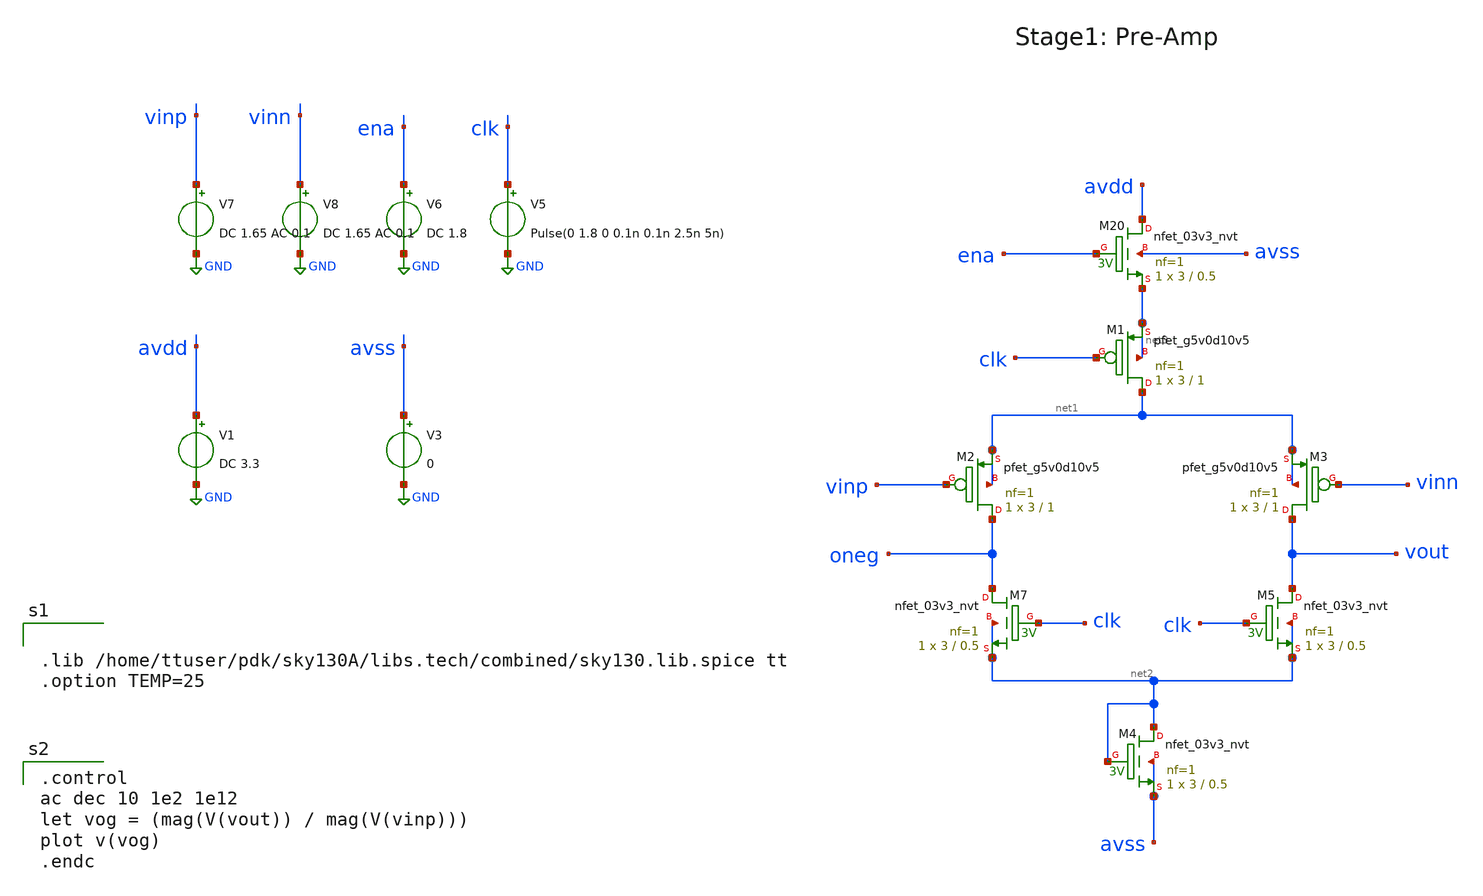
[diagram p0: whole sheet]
** sch_path: xschem/preamp.sch
**.subckt preamp
XM1 net1 clk net3 net3 sky130_fd_pr__pfet_g5v0d10v5 L=1 W=3 nf=1 ad='int((nf+1)/2) * W/nf * 0.29' as='int((nf+2)/2) * W/nf * 0.29'
+ pd='2*int((nf+1)/2) * (W/nf + 0.29)' ps='2*int((nf+2)/2) * (W/nf + 0.29)' nrd='0.29 / W' nrs='0.29 / W'
+ sa=0 sb=0 sd=0 mult=1 m=1
XM2 oneg vinp net1 net1 sky130_fd_pr__pfet_g5v0d10v5 L=1 W=3 nf=1 ad='int((nf+1)/2) * W/nf * 0.29' as='int((nf+2)/2) * W/nf * 0.29'
+ pd='2*int((nf+1)/2) * (W/nf + 0.29)' ps='2*int((nf+2)/2) * (W/nf + 0.29)' nrd='0.29 / W' nrs='0.29 / W'
+ sa=0 sb=0 sd=0 mult=1 m=1
XM3 vout vinn net1 net1 sky130_fd_pr__pfet_g5v0d10v5 L=1 W=3 nf=1 ad='int((nf+1)/2) * W/nf * 0.29' as='int((nf+2)/2) * W/nf * 0.29'
+ pd='2*int((nf+1)/2) * (W/nf + 0.29)' ps='2*int((nf+2)/2) * (W/nf + 0.29)' nrd='0.29 / W' nrs='0.29 / W'
+ sa=0 sb=0 sd=0 mult=1 m=1
XM7 oneg clk net2 net2 sky130_fd_pr__nfet_03v3_nvt L=0.5 W=3 nf=1 ad='int((nf+1)/2) * W/nf * 0.29' as='int((nf+2)/2) * W/nf * 0.29'
+ pd='2*int((nf+1)/2) * (W/nf + 0.29)' ps='2*int((nf+2)/2) * (W/nf + 0.29)' nrd='0.29 / W' nrs='0.29 / W'
+ sa=0 sb=0 sd=0 mult=1 m=1
XM5 vout clk net2 net2 sky130_fd_pr__nfet_03v3_nvt L=0.5 W=3 nf=1 ad='int((nf+1)/2) * W/nf * 0.29' as='int((nf+2)/2) * W/nf * 0.29'
+ pd='2*int((nf+1)/2) * (W/nf + 0.29)' ps='2*int((nf+2)/2) * (W/nf + 0.29)' nrd='0.29 / W' nrs='0.29 / W'
+ sa=0 sb=0 sd=0 mult=1 m=1
XM4 net2 net2 avss avss sky130_fd_pr__nfet_03v3_nvt L=0.5 W=3 nf=1 ad='int((nf+1)/2) * W/nf * 0.29' as='int((nf+2)/2) * W/nf * 0.29'
+ pd='2*int((nf+1)/2) * (W/nf + 0.29)' ps='2*int((nf+2)/2) * (W/nf + 0.29)' nrd='0.29 / W' nrs='0.29 / W'
+ sa=0 sb=0 sd=0 mult=1 m=1
XM20 avdd ena net3 avss sky130_fd_pr__nfet_03v3_nvt L=0.5 W=3 nf=1 ad='int((nf+1)/2) * W/nf * 0.29' as='int((nf+2)/2) * W/nf * 0.29'
+ pd='2*int((nf+1)/2) * (W/nf + 0.29)' ps='2*int((nf+2)/2) * (W/nf + 0.29)' nrd='0.29 / W' nrs='0.29 / W'
+ sa=0 sb=0 sd=0 mult=1 m=1
V1 avdd GND DC 3.3
V3 avss GND 0
V5 clk GND Pulse(0 1.8 0 0.1n 0.1n 2.5n 5n)
V6 ena GND DC 1.8
V7 vinp GND DC 1.65 AC 0.1
V8 vinn GND DC 1.65 AC 0.1
**** begin user architecture code


.lib /home/ttuser/pdk/sky130A/libs.tech/combined/sky130.lib.spice tt
.option TEMP=25


.control
ac dec 10 1e2 1e12
let vog = (mag(V(vout)) / mag(V(vinp)))
plot v(vog)
.endc

**** end user architecture code
**.ends
.GLOBAL GND
.end
